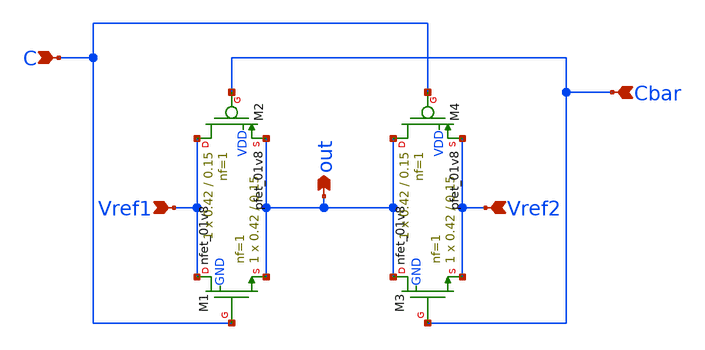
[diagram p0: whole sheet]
** sch_path: xschem/mux/analogMux.sch
**.subckt analogMux Vref1 out Vref2 C Cbar
*.ipin Vref1
*.opin out
*.ipin Vref2
*.ipin C
*.ipin Cbar
XM1 Vref1 C out GND sky130_fd_pr__nfet_01v8 L=0.15 W=0.42 nf=1 ad='int((nf+1)/2) * W/nf * 0.29' as='int((nf+2)/2) * W/nf * 0.29'
+ pd='2*int((nf+1)/2) * (W/nf + 0.29)' ps='2*int((nf+2)/2) * (W/nf + 0.29)' nrd='0.29 / W' nrs='0.29 / W'
+ sa=0 sb=0 sd=0 mult=1 m=1
XM2 Vref1 Cbar out VDD sky130_fd_pr__pfet_01v8 L=0.15 W=0.42 nf=1 ad='int((nf+1)/2) * W/nf * 0.29' as='int((nf+2)/2) * W/nf * 0.29'
+ pd='2*int((nf+1)/2) * (W/nf + 0.29)' ps='2*int((nf+2)/2) * (W/nf + 0.29)' nrd='0.29 / W' nrs='0.29 / W'
+ sa=0 sb=0 sd=0 mult=1 m=1
XM3 out Cbar Vref2 GND sky130_fd_pr__nfet_01v8 L=0.15 W=0.42 nf=1 ad='int((nf+1)/2) * W/nf * 0.29' as='int((nf+2)/2) * W/nf * 0.29'
+ pd='2*int((nf+1)/2) * (W/nf + 0.29)' ps='2*int((nf+2)/2) * (W/nf + 0.29)' nrd='0.29 / W' nrs='0.29 / W'
+ sa=0 sb=0 sd=0 mult=1 m=1
XM4 out C Vref2 VDD sky130_fd_pr__pfet_01v8 L=0.15 W=0.42 nf=1 ad='int((nf+1)/2) * W/nf * 0.29' as='int((nf+2)/2) * W/nf * 0.29'
+ pd='2*int((nf+1)/2) * (W/nf + 0.29)' ps='2*int((nf+2)/2) * (W/nf + 0.29)' nrd='0.29 / W' nrs='0.29 / W'
+ sa=0 sb=0 sd=0 mult=1 m=1
**.ends
.end
